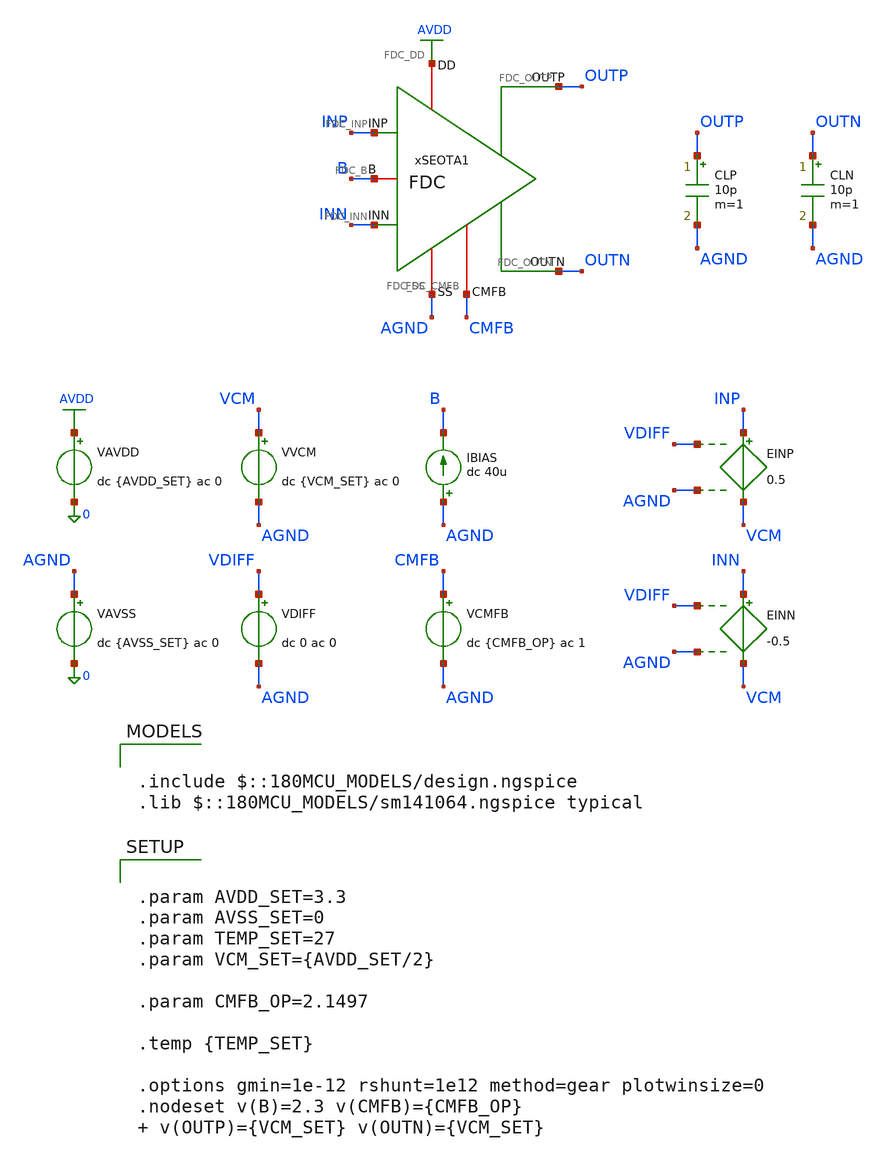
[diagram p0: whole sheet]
** sch_path: Design_Files/IC Design/Testbench/FD_OTA/FDC/Open_Loop/FDC_TB_PLANT_NOM.sch
**.subckt FDC_TB_PLANT_NOM
IBIAS AGND B dc 40u
VAVDD AVDD 0 dc {AVDD_SET} ac 0
.save i(vavdd)
CLP OUTP AGND 10p m=1
VVCM VCM AGND dc {VCM_SET} ac 0
VDIFF VDIFF AGND dc 0 ac 0
VAVSS AGND 0 dc {AVSS_SET} ac 0
.save i(vavss)
EINN INN VCM VDIFF AGND -0.5
EINP INP VCM VDIFF AGND 0.5
xSEOTA1 AVDD AGND INP INN OUTN B OUTP CMFB FDC
CLN OUTN AGND 10p m=1
VCMFB CMFB AGND dc {CMFB_OP} ac 1
**** begin user architecture code

.include $::180MCU_MODELS/design.ngspice
.lib $::180MCU_MODELS/sm141064.ngspice typical



.control
destroy all
save all
set wr_vecnames
set wr_singlescale
option numdgt=15

shell mkdir -p
+ /foss/designs/ECG_Acquisition_IC/Measurement_Results/IC_Simulation/FD_OTA/FDC/NOM.Result_txt

shell rm -f
+ /foss/designs/ECG_Acquisition_IC/Measurement_Results/IC_Simulation/FD_OTA/FDC/NOM.Result_txt/NOM.plant_ac.txt

alter @VAVDD[ACMAG]  = 0
alter @VAVSS[ACMAG]  = 0
alter @VVCM[ACMAG]   = 0
alter @VDIFF[ACMAG]  = 0

alter @VCMFB[ACMAG]   = 1
alter @VCMFB[ACPHASE] = 0

ac dec 200 0.1 1G

let vcmfb_ac  = v(cmfb)-v(agnd)
let voutp_ac  = v(outp)-v(agnd)
let voutn_ac  = v(outn)-v(agnd)
let voutcm_ac = (voutp_ac+voutn_ac)/2

let plant_ac   = voutcm_ac/vcmfb_ac
let plant_real = real(plant_ac)
let plant_imag = imag(plant_ac)

setscale frequency

wrdata
+ /foss/designs/ECG_Acquisition_IC/Measurement_Results/IC_Simulation/FD_OTA/FDC/NOM.Result_txt/NOM.plant_ac.txt plant_real plant_imag

quit
.endc




.param AVDD_SET=3.3
.param AVSS_SET=0
.param TEMP_SET=27
.param VCM_SET={AVDD_SET/2}

.param CMFB_OP=2.1497

.temp {TEMP_SET}

.options gmin=1e-12 rshunt=1e12 method=gear plotwinsize=0
.nodeset v(B)=2.3 v(CMFB)={CMFB_OP}  v(OUTP)={VCM_SET} v(OUTN)={VCM_SET}


**** end user architecture code
**.ends

* expanding   symbol:  ECG_Acquisition_IC/Design_Files/IC Design/Schematic/FD_OTA/FDC/FDC.sym # of
*+ pins=8
** sym_path: Design_Files/IC Design/Schematic/FD_OTA/FDC/FDC.sym
** sch_path: Design_Files/IC Design/Schematic/FD_OTA/FDC/FDC.sch
.subckt FDC FDC_DD FDC_SS FDC_INP FDC_INN FDC_OUTN FDC_B FDC_OUTP FDC_CMFB
*.iopin FDC_DD
*.iopin FDC_SS
*.ipin FDC_INP
*.ipin FDC_INN
*.opin FDC_OUTP
*.iopin FDC_B
*.opin FDC_OUTN
*.iopin FDC_CMFB
XM3 net4 FDC_CMFB FDC_DD FDC_DD pfet_03v3 L=2u W=1u nf=1 ad='int((nf+1)/2) * W/nf * 0.18u' as='int((nf+2)/2) * W/nf * 0.18u'
+ pd='2*int((nf+1)/2) * (W/nf + 0.18u)' ps='2*int((nf+2)/2) * (W/nf + 0.18u)' nrd='0.18u / W' nrs='0.18u / W'
+ sa=0 sb=0 sd=0 m=200
XM8 FDC_OUTP FDC_B FDC_SS FDC_SS nfet_03v3 L=1u W=1u nf=1 ad='int((nf+1)/2) * W/nf * 0.18u' as='int((nf+2)/2) * W/nf * 0.18u'
+ pd='2*int((nf+1)/2) * (W/nf + 0.18u)' ps='2*int((nf+2)/2) * (W/nf + 0.18u)' nrd='0.18u / W' nrs='0.18u / W'
+ sa=0 sb=0 sd=0 m=200
Rz net1 net2 6k m=1
XM5 net3 FDC_B FDC_SS FDC_SS nfet_03v3 L=2u W=1u nf=1 ad='int((nf+1)/2) * W/nf * 0.18u' as='int((nf+2)/2) * W/nf * 0.18u'
+ pd='2*int((nf+1)/2) * (W/nf + 0.18u)' ps='2*int((nf+2)/2) * (W/nf + 0.18u)' nrd='0.18u / W' nrs='0.18u / W'
+ sa=0 sb=0 sd=0 m=10
XM6 FDC_OUTP net1 FDC_DD FDC_DD pfet_03v3 L=1u W=1u nf=1 ad='int((nf+1)/2) * W/nf * 0.18u' as='int((nf+2)/2) * W/nf * 0.18u'
+ pd='2*int((nf+1)/2) * (W/nf + 0.18u)' ps='2*int((nf+2)/2) * (W/nf + 0.18u)' nrd='0.18u / W' nrs='0.18u / W'
+ sa=0 sb=0 sd=0 m=200
XM10 FDC_B FDC_B FDC_SS FDC_SS nfet_03v3 L=2u W=1u nf=1 ad='int((nf+1)/2) * W/nf * 0.18u' as='int((nf+2)/2) * W/nf * 0.18u'
+ pd='2*int((nf+1)/2) * (W/nf + 0.18u)' ps='2*int((nf+2)/2) * (W/nf + 0.18u)' nrd='0.18u / W' nrs='0.18u / W'
+ sa=0 sb=0 sd=0 m=20
Cc net2 FDC_OUTP 3p m=1
XM9 FDC_OUTN FDC_B FDC_SS FDC_SS nfet_03v3 L=1u W=1u nf=1 ad='int((nf+1)/2) * W/nf * 0.18u' as='int((nf+2)/2) * W/nf * 0.18u'
+ pd='2*int((nf+1)/2) * (W/nf + 0.18u)' ps='2*int((nf+2)/2) * (W/nf + 0.18u)' nrd='0.18u / W' nrs='0.18u / W'
+ sa=0 sb=0 sd=0 m=200
Rz1 net4 net5 6k m=1
XM7 FDC_OUTN net4 FDC_DD FDC_DD pfet_03v3 L=1u W=1u nf=1 ad='int((nf+1)/2) * W/nf * 0.18u' as='int((nf+2)/2) * W/nf * 0.18u'
+ pd='2*int((nf+1)/2) * (W/nf + 0.18u)' ps='2*int((nf+2)/2) * (W/nf + 0.18u)' nrd='0.18u / W' nrs='0.18u / W'
+ sa=0 sb=0 sd=0 m=200
Cc1 net5 FDC_OUTN 3p m=1
XM4 net1 FDC_CMFB FDC_DD FDC_DD pfet_03v3 L=2u W=1u nf=1 ad='int((nf+1)/2) * W/nf * 0.18u' as='int((nf+2)/2) * W/nf * 0.18u'
+ pd='2*int((nf+1)/2) * (W/nf + 0.18u)' ps='2*int((nf+2)/2) * (W/nf + 0.18u)' nrd='0.18u / W' nrs='0.18u / W'
+ sa=0 sb=0 sd=0 m=200
XM1 net4 FDC_INN net3 FDC_SS nfet_03v3 L=2u W=1u nf=1 ad='int((nf+1)/2) * W/nf * 0.18u' as='int((nf+2)/2) * W/nf * 0.18u'
+ pd='2*int((nf+1)/2) * (W/nf + 0.18u)' ps='2*int((nf+2)/2) * (W/nf + 0.18u)' nrd='0.18u / W' nrs='0.18u / W'
+ sa=0 sb=0 sd=0 m=200
XM2 net1 FDC_INP net3 FDC_SS nfet_03v3 L=2u W=1u nf=1 ad='int((nf+1)/2) * W/nf * 0.18u' as='int((nf+2)/2) * W/nf * 0.18u'
+ pd='2*int((nf+1)/2) * (W/nf + 0.18u)' ps='2*int((nf+2)/2) * (W/nf + 0.18u)' nrd='0.18u / W' nrs='0.18u / W'
+ sa=0 sb=0 sd=0 m=200
.ends

.GLOBAL AVDD
.end
